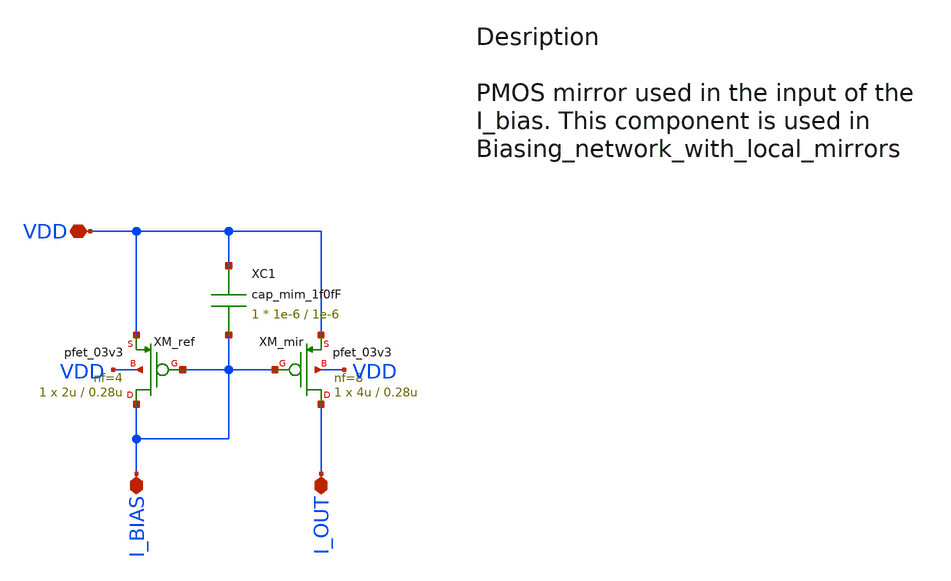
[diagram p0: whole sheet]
** sch_path: src/python/Cmirror_with_decap/xschem/pmos_Cmirror_with_decap.sch
**.subckt pmos_Cmirror_with_decap I_BIAS VDD I_OUT
*.iopin I_BIAS
*.iopin VDD
*.iopin I_OUT
XC1 VDD I_BIAS cap_mim_1f0fF c_width=1e-6 c_length=1e-6 m=1
XM_ref I_BIAS I_BIAS VDD VDD pfet_03v3 L=0.28u W=2u nf=4 ad='int((nf+1)/2) * W/nf * 0.18u' as='int((nf+2)/2) * W/nf * 0.18u'
+ pd='2*int((nf+1)/2) * (W/nf + 0.18u)' ps='2*int((nf+2)/2) * (W/nf + 0.18u)' nrd='0.18u / W' nrs='0.18u / W'
+ sa=0 sb=0 sd=0 m=1
XM_mir I_OUT I_BIAS VDD VDD pfet_03v3 L=0.28u W=4u nf=8 ad='int((nf+1)/2) * W/nf * 0.18u' as='int((nf+2)/2) * W/nf * 0.18u'
+ pd='2*int((nf+1)/2) * (W/nf + 0.18u)' ps='2*int((nf+2)/2) * (W/nf + 0.18u)' nrd='0.18u / W' nrs='0.18u / W'
+ sa=0 sb=0 sd=0 m=1
**** begin user architecture code

.include $::180MCU_MODELS/design.ngspice
.lib $::180MCU_MODELS/sm141064.ngspice typical
.lib $::180MCU_MODELS/sm141064.ngspice cap_mim
.lib $::180MCU_MODELS/sm141064.ngspice res_typical




* let sets vectors to a plot, while set sets a variable, globally accessible in .control
.control

    * Set frequency and amplitude variables to proper values from within the control sequence
    save all

    op
    show

    write Biasing_network_sim.raw

    set appendwrite

    * Transient analysis to observe mixing operation
    tran 1p 10n


    write Biasing_network_sim.raw

.endc


**** end user architecture code
**.ends
.end
